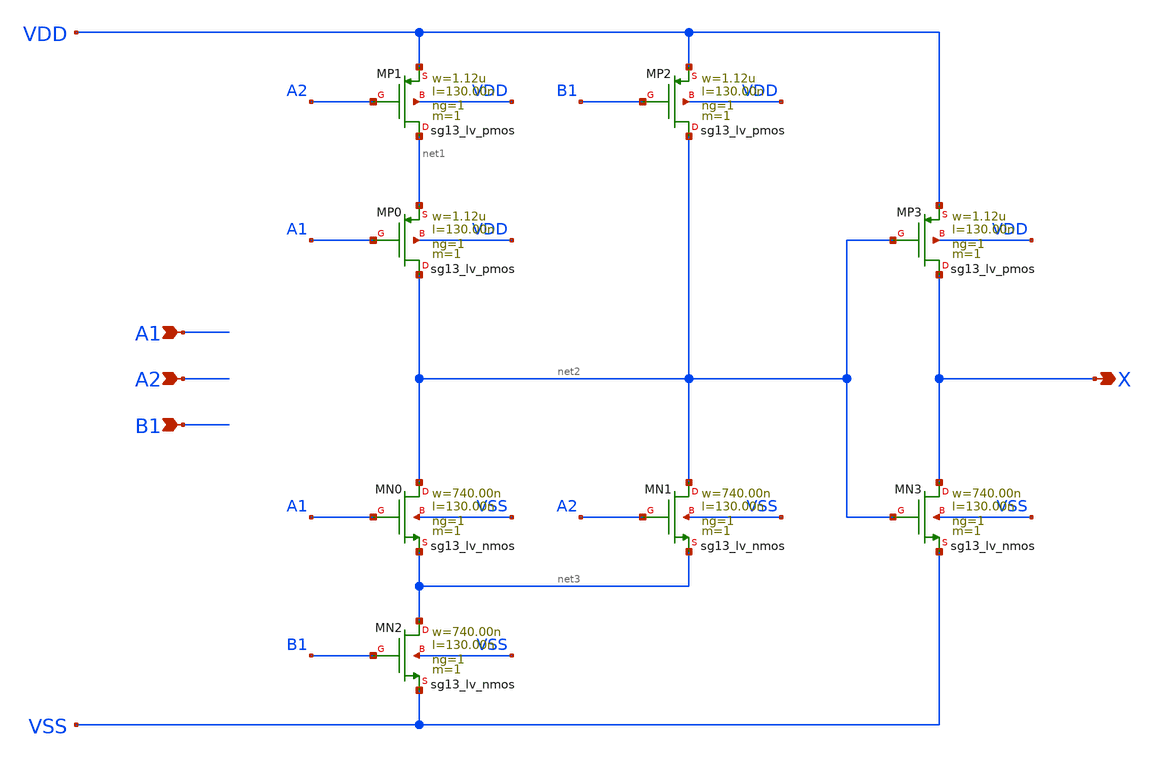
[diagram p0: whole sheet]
** sch_path: outputs/sg13g2_cells/cells/sg13g2_o21a_1/sg13g2_o21a_1.sch
**.subckt sg13g2_o21a_1 A1 A2 B1 X
*.ipin A1
*.ipin A2
*.ipin B1
*.opin X
XMN0 net2 A1 net3 VSS sg13_lv_nmos w=740.00n l=130.00n ng=1 m=1 mm_ok=1
XMN1 net2 A2 net3 VSS sg13_lv_nmos w=740.00n l=130.00n ng=1 m=1 mm_ok=1
XMN2 net3 B1 VSS VSS sg13_lv_nmos w=740.00n l=130.00n ng=1 m=1 mm_ok=1
XMN3 X net2 VSS VSS sg13_lv_nmos w=740.00n l=130.00n ng=1 m=1 mm_ok=1
XMP0 net2 A1 net1 VDD sg13_lv_pmos w=1.12u l=130.00n ng=1 m=1 mm_ok=1
XMP1 net1 A2 VDD VDD sg13_lv_pmos w=1.12u l=130.00n ng=1 m=1 mm_ok=1
XMP2 net2 B1 VDD VDD sg13_lv_pmos w=1.12u l=130.00n ng=1 m=1 mm_ok=1
XMP3 X net2 VDD VDD sg13_lv_pmos w=1.12u l=130.00n ng=1 m=1 mm_ok=1
**.ends
.end
